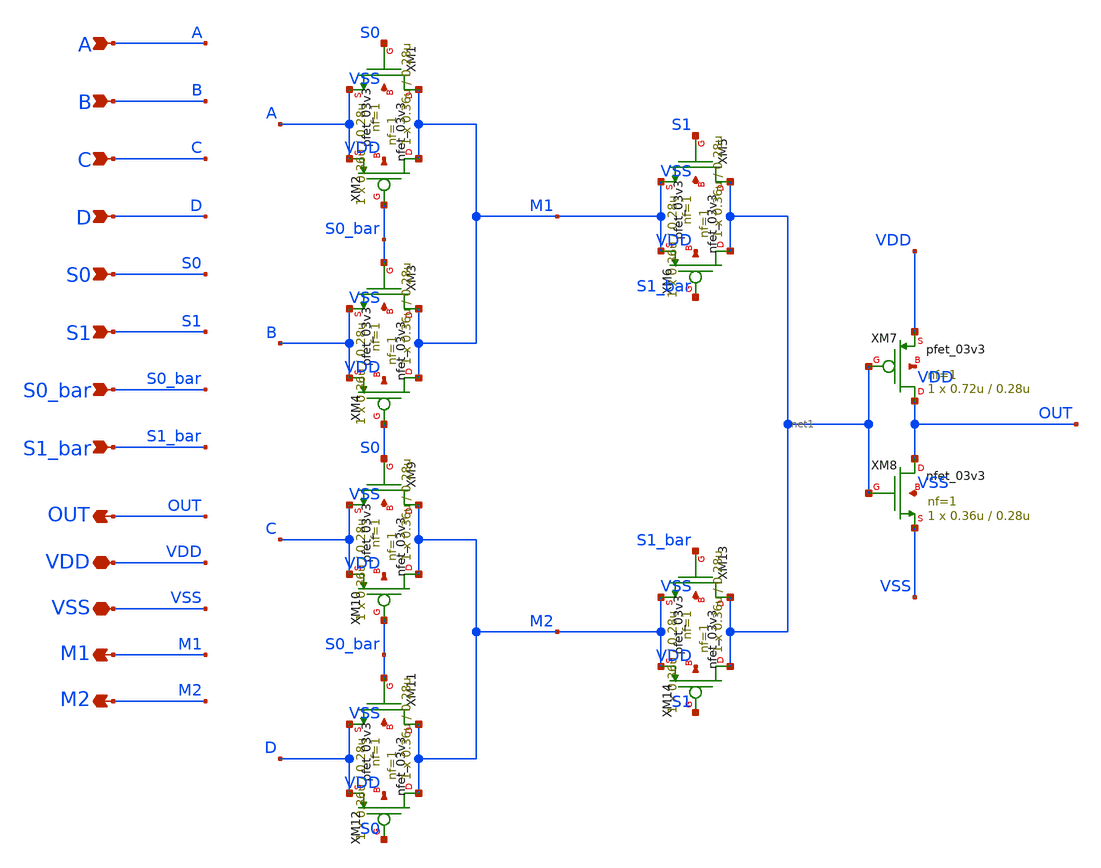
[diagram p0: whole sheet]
** sch_path: CAD4/4to1MUX_6TG.sch
**.subckt 4to1MUX_6TG A B S0 C D OUT S1 VDD VSS S0_bar S1_bar M1 M2
*.ipin A
*.ipin B
*.ipin S0
*.ipin C
*.ipin D
*.opin OUT
*.ipin S1
*.iopin VDD
*.iopin VSS
*.ipin S0_bar
*.ipin S1_bar
*.opin M1
*.opin M2
XM1 M1 S0 A VSS nfet_03v3 L=0.28u W=0.36u nf=1 ad='int((nf+1)/2) * W/nf * 0.18u' as='int((nf+2)/2) * W/nf * 0.18u'
+ pd='2*int((nf+1)/2) * (W/nf + 0.18u)' ps='2*int((nf+2)/2) * (W/nf + 0.18u)' nrd='0.18u / W' nrs='0.18u / W'
+ sa=0 sb=0 sd=0 m=1
XM2 M1 S0_bar A VDD pfet_03v3 L=0.28u W=0.36u nf=1 ad='int((nf+1)/2) * W/nf * 0.18u' as='int((nf+2)/2) * W/nf * 0.18u'
+ pd='2*int((nf+1)/2) * (W/nf + 0.18u)' ps='2*int((nf+2)/2) * (W/nf + 0.18u)' nrd='0.18u / W' nrs='0.18u / W'
+ sa=0 sb=0 sd=0 m=1
XM3 M1 S0_bar B VSS nfet_03v3 L=0.28u W=0.36u nf=1 ad='int((nf+1)/2) * W/nf * 0.18u' as='int((nf+2)/2) * W/nf * 0.18u'
+ pd='2*int((nf+1)/2) * (W/nf + 0.18u)' ps='2*int((nf+2)/2) * (W/nf + 0.18u)' nrd='0.18u / W' nrs='0.18u / W'
+ sa=0 sb=0 sd=0 m=1
XM4 M1 S0 B VDD pfet_03v3 L=0.28u W=0.36u nf=1 ad='int((nf+1)/2) * W/nf * 0.18u' as='int((nf+2)/2) * W/nf * 0.18u'
+ pd='2*int((nf+1)/2) * (W/nf + 0.18u)' ps='2*int((nf+2)/2) * (W/nf + 0.18u)' nrd='0.18u / W' nrs='0.18u / W'
+ sa=0 sb=0 sd=0 m=1
XM5 net1 S1 M1 VSS nfet_03v3 L=0.28u W=0.36u nf=1 ad='int((nf+1)/2) * W/nf * 0.18u' as='int((nf+2)/2) * W/nf * 0.18u'
+ pd='2*int((nf+1)/2) * (W/nf + 0.18u)' ps='2*int((nf+2)/2) * (W/nf + 0.18u)' nrd='0.18u / W' nrs='0.18u / W'
+ sa=0 sb=0 sd=0 m=1
XM6 net1 S1_bar M1 VDD pfet_03v3 L=0.28u W=0.36u nf=1 ad='int((nf+1)/2) * W/nf * 0.18u' as='int((nf+2)/2) * W/nf * 0.18u'
+ pd='2*int((nf+1)/2) * (W/nf + 0.18u)' ps='2*int((nf+2)/2) * (W/nf + 0.18u)' nrd='0.18u / W' nrs='0.18u / W'
+ sa=0 sb=0 sd=0 m=1
XM7 OUT net1 VDD VDD pfet_03v3 L=0.28u W=0.72u nf=1 ad='int((nf+1)/2) * W/nf * 0.18u' as='int((nf+2)/2) * W/nf * 0.18u'
+ pd='2*int((nf+1)/2) * (W/nf + 0.18u)' ps='2*int((nf+2)/2) * (W/nf + 0.18u)' nrd='0.18u / W' nrs='0.18u / W'
+ sa=0 sb=0 sd=0 m=1
XM8 OUT net1 VSS VSS nfet_03v3 L=0.28u W=0.36u nf=1 ad='int((nf+1)/2) * W/nf * 0.18u' as='int((nf+2)/2) * W/nf * 0.18u'
+ pd='2*int((nf+1)/2) * (W/nf + 0.18u)' ps='2*int((nf+2)/2) * (W/nf + 0.18u)' nrd='0.18u / W' nrs='0.18u / W'
+ sa=0 sb=0 sd=0 m=1
XM9 M2 S0 C VSS nfet_03v3 L=0.28u W=0.36u nf=1 ad='int((nf+1)/2) * W/nf * 0.18u' as='int((nf+2)/2) * W/nf * 0.18u'
+ pd='2*int((nf+1)/2) * (W/nf + 0.18u)' ps='2*int((nf+2)/2) * (W/nf + 0.18u)' nrd='0.18u / W' nrs='0.18u / W'
+ sa=0 sb=0 sd=0 m=1
XM10 M2 S0_bar C VDD pfet_03v3 L=0.28u W=0.36u nf=1 ad='int((nf+1)/2) * W/nf * 0.18u' as='int((nf+2)/2) * W/nf * 0.18u'
+ pd='2*int((nf+1)/2) * (W/nf + 0.18u)' ps='2*int((nf+2)/2) * (W/nf + 0.18u)' nrd='0.18u / W' nrs='0.18u / W'
+ sa=0 sb=0 sd=0 m=1
XM11 M2 S0_bar D VSS nfet_03v3 L=0.28u W=0.36u nf=1 ad='int((nf+1)/2) * W/nf * 0.18u' as='int((nf+2)/2) * W/nf * 0.18u'
+ pd='2*int((nf+1)/2) * (W/nf + 0.18u)' ps='2*int((nf+2)/2) * (W/nf + 0.18u)' nrd='0.18u / W' nrs='0.18u / W'
+ sa=0 sb=0 sd=0 m=1
XM12 M2 S0 D VDD pfet_03v3 L=0.28u W=0.36u nf=1 ad='int((nf+1)/2) * W/nf * 0.18u' as='int((nf+2)/2) * W/nf * 0.18u'
+ pd='2*int((nf+1)/2) * (W/nf + 0.18u)' ps='2*int((nf+2)/2) * (W/nf + 0.18u)' nrd='0.18u / W' nrs='0.18u / W'
+ sa=0 sb=0 sd=0 m=1
XM13 net1 S1_bar M2 VSS nfet_03v3 L=0.28u W=0.36u nf=1 ad='int((nf+1)/2) * W/nf * 0.18u' as='int((nf+2)/2) * W/nf * 0.18u'
+ pd='2*int((nf+1)/2) * (W/nf + 0.18u)' ps='2*int((nf+2)/2) * (W/nf + 0.18u)' nrd='0.18u / W' nrs='0.18u / W'
+ sa=0 sb=0 sd=0 m=1
XM14 net1 S1 M2 VDD pfet_03v3 L=0.28u W=0.36u nf=1 ad='int((nf+1)/2) * W/nf * 0.18u' as='int((nf+2)/2) * W/nf * 0.18u'
+ pd='2*int((nf+1)/2) * (W/nf + 0.18u)' ps='2*int((nf+2)/2) * (W/nf + 0.18u)' nrd='0.18u / W' nrs='0.18u / W'
+ sa=0 sb=0 sd=0 m=1
**.ends
.end
